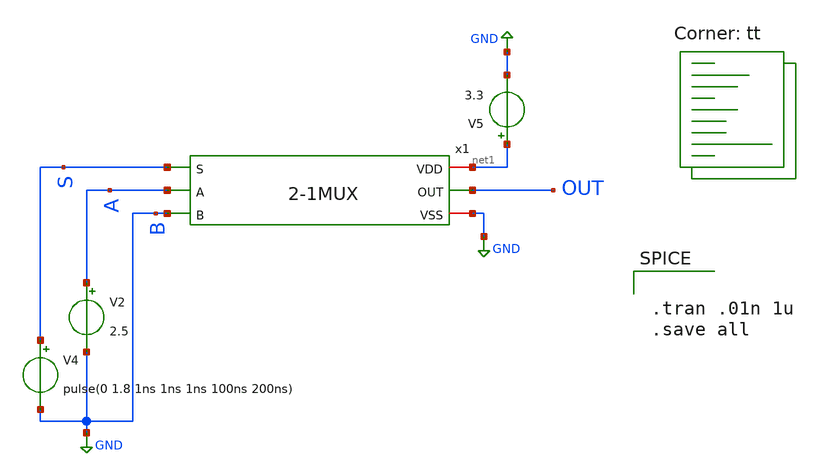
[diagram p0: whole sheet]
** sch_path: xschem/Testbenches/2-1MUXTB.sch
**.subckt 2-1MUXTB
V2 A GND 2.5
V5 net1 GND 3.3
V4 S GND pulse(0 1.8 1ns 1ns 1ns 100ns 200ns)
x1 net1 S A OUT GND GND 2-1MUX
**** begin user architecture code
.lib $::SKYWATER_MODELS/sky130.lib.spice tt


.tran .01n 1u
.save all

**** end user architecture code
**.ends

* expanding   symbol:  2-1MUX.sym # of pins=6
** sym_path: xschem/2-1MUX.sym
** sch_path: xschem/2-1MUX.sch
.subckt 2-1MUX VDD S A OUT B VSS
*.ipin A
*.ipin B
*.ipin S
*.iopin VDD
*.iopin VSS
*.opin OUT
x1 net1 VDD OUT A VSS S TransmissionGate
x2 S VDD OUT B VSS net1 TransmissionGate
x3 VDD S net1 VSS Inverter
.ends


* expanding   symbol:  TransmissionGate.sym # of pins=6
** sym_path: xschem/TransmissionGate.sym
** sch_path: xschem/TransmissionGate.sch
.subckt TransmissionGate SP VDD Out In VSS SN
*.opin Out
*.ipin In
*.ipin SP
*.iopin VDD
*.iopin VSS
*.ipin SN
XM1 In SN Out VSS sky130_fd_pr__nfet_g5v0d10v5 L=0.5 W=0.75 nf=1 ad='int((nf+1)/2) * W/nf * 0.29' as='int((nf+2)/2) * W/nf * 0.29'
+ pd='2*int((nf+1)/2) * (W/nf + 0.29)' ps='2*int((nf+2)/2) * (W/nf + 0.29)' nrd='0.29 / W' nrs='0.29 / W'
+ sa=0 sb=0 sd=0 mult=1 m=1
XM2 In SP Out VDD sky130_fd_pr__pfet_g5v0d10v5 L=0.5 W=1.5 nf=1 ad='int((nf+1)/2) * W/nf * 0.29' as='int((nf+2)/2) * W/nf * 0.29'
+ pd='2*int((nf+1)/2) * (W/nf + 0.29)' ps='2*int((nf+2)/2) * (W/nf + 0.29)' nrd='0.29 / W' nrs='0.29 / W'
+ sa=0 sb=0 sd=0 mult=1 m=1
.ends


* expanding   symbol:  Inverter.sym # of pins=4
** sym_path: xschem/Inverter.sym
** sch_path: xschem/Inverter.sch
.subckt Inverter VDD Vin Vout VSS
*.ipin Vin
*.iopin VDD
*.iopin VSS
*.opin Vout
XM1 Vout Vin VSS VSS sky130_fd_pr__nfet_g5v0d10v5 L=0.5 W=0.75 nf=1 ad='int((nf+1)/2) * W/nf * 0.29'
+ as='int((nf+2)/2) * W/nf * 0.29' pd='2*int((nf+1)/2) * (W/nf + 0.29)' ps='2*int((nf+2)/2) * (W/nf + 0.29)'
+ nrd='0.29 / W' nrs='0.29 / W' sa=0 sb=0 sd=0 mult=1 m=1
XM2 Vout Vin VDD VDD sky130_fd_pr__pfet_g5v0d10v5 L=0.5 W=1.5 nf=1 ad='int((nf+1)/2) * W/nf * 0.29' as='int((nf+2)/2) * W/nf * 0.29'
+ pd='2*int((nf+1)/2) * (W/nf + 0.29)' ps='2*int((nf+2)/2) * (W/nf + 0.29)' nrd='0.29 / W' nrs='0.29 / W'
+ sa=0 sb=0 sd=0 mult=1 m=1
.ends

.GLOBAL GND
.end
